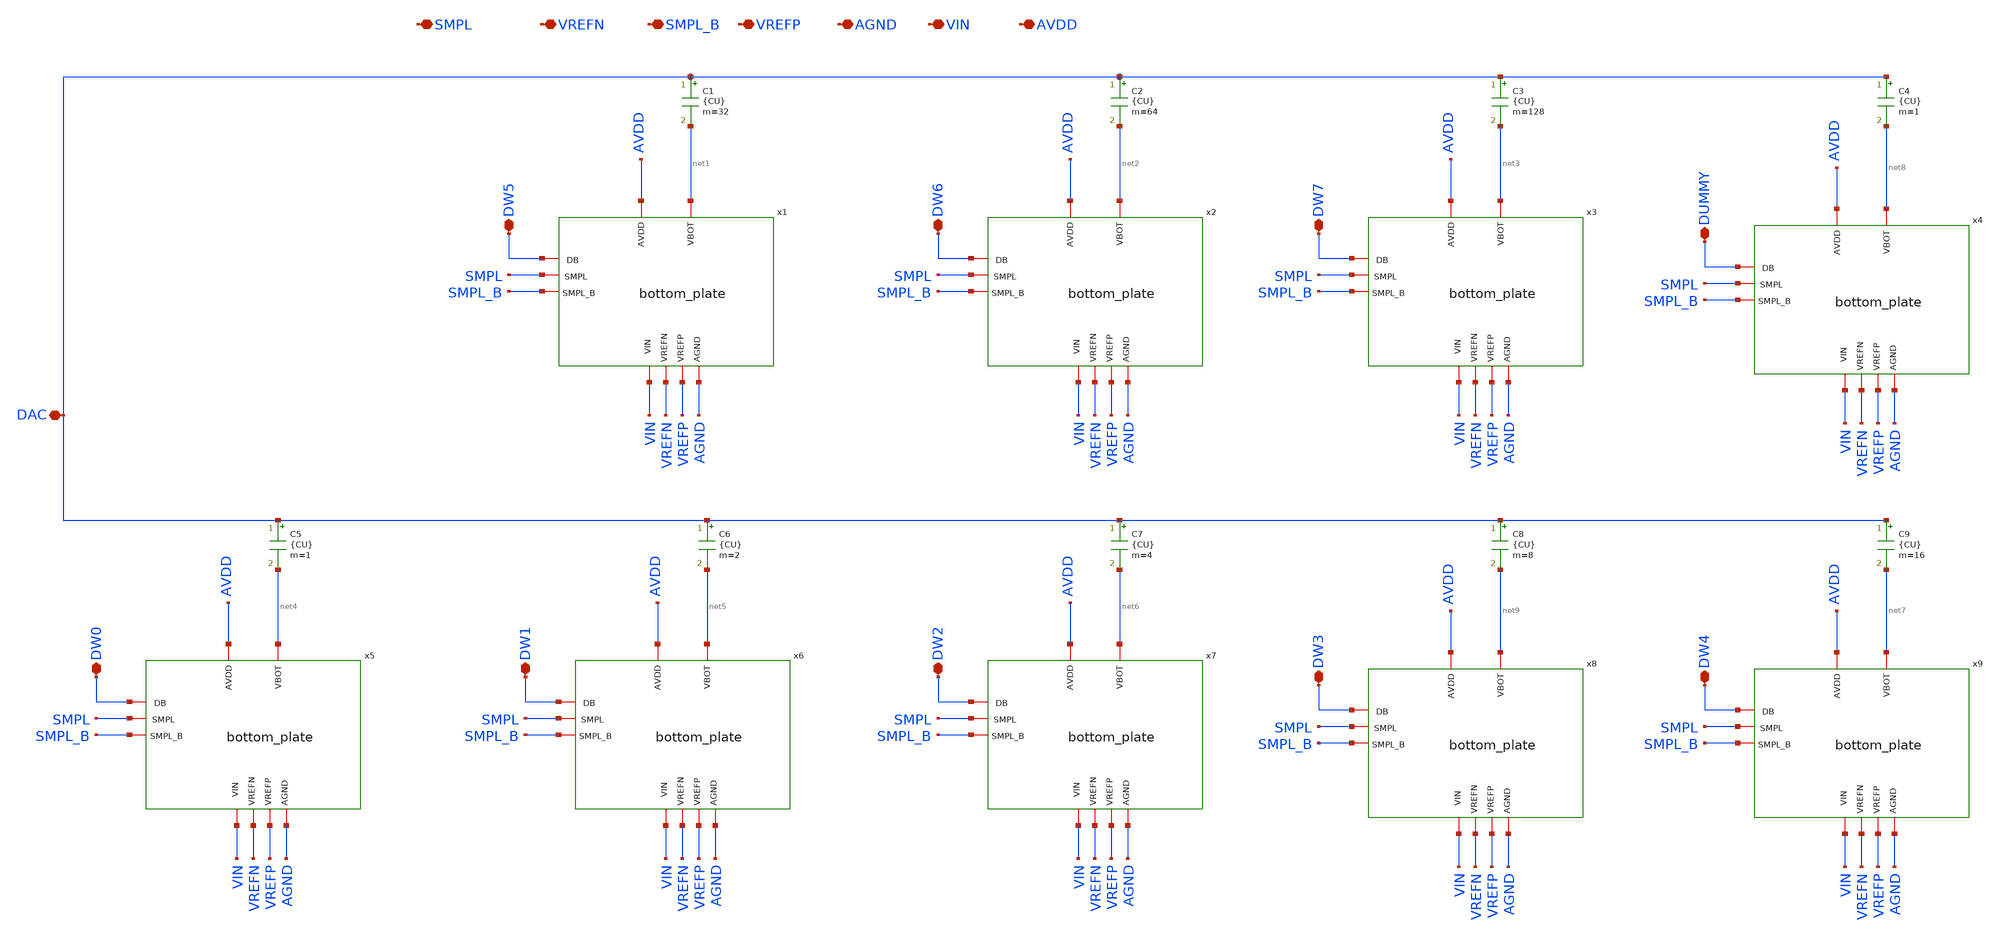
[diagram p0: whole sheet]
** sch_path: Designs/capacitive_DAC.sch
**.subckt capacitive_DAC DW5 DW6 DW7 DUMMY DW0 DW1 DW2 DW3 DW4 DAC SMPL VREFN SMPL_B VREFP AGND VIN
*+ AVDD
*.iopin DW5
*.iopin DW6
*.iopin DW7
*.iopin DUMMY
*.iopin DW0
*.iopin DW1
*.iopin DW2
*.iopin DW3
*.iopin DW4
*.iopin DAC
*.iopin SMPL
*.iopin VREFN
*.iopin SMPL_B
*.iopin VREFP
*.iopin AGND
*.iopin VIN
*.iopin AVDD
x1 net1 VREFP VREFN AGND AVDD VIN SMPL SMPL_B DW5 bottom_plate
C1 DAC net1 {CU} m=32
x2 net2 VREFP VREFN AGND AVDD VIN SMPL SMPL_B DW6 bottom_plate
C2 DAC net2 {CU} m=64
x3 net3 VREFP VREFN AGND AVDD VIN SMPL SMPL_B DW7 bottom_plate
C3 DAC net3 {CU} m=128
x4 net8 VREFP VREFN AGND AVDD VIN SMPL SMPL_B DUMMY bottom_plate
C4 DAC net8 {CU} m=1
x5 net4 VREFP VREFN AGND AVDD VIN SMPL SMPL_B DW0 bottom_plate
C5 DAC net4 {CU} m=1
x6 net5 VREFP VREFN AGND AVDD VIN SMPL SMPL_B DW1 bottom_plate
C6 DAC net5 {CU} m=2
x7 net6 VREFP VREFN AGND AVDD VIN SMPL SMPL_B DW2 bottom_plate
C7 DAC net6 {CU} m=4
x8 net9 VREFP VREFN AGND AVDD VIN SMPL SMPL_B DW3 bottom_plate
C8 DAC net9 {CU} m=8
x9 net7 VREFP VREFN AGND AVDD VIN SMPL SMPL_B DW4 bottom_plate
C9 DAC net7 {CU} m=16
**.ends
.end
